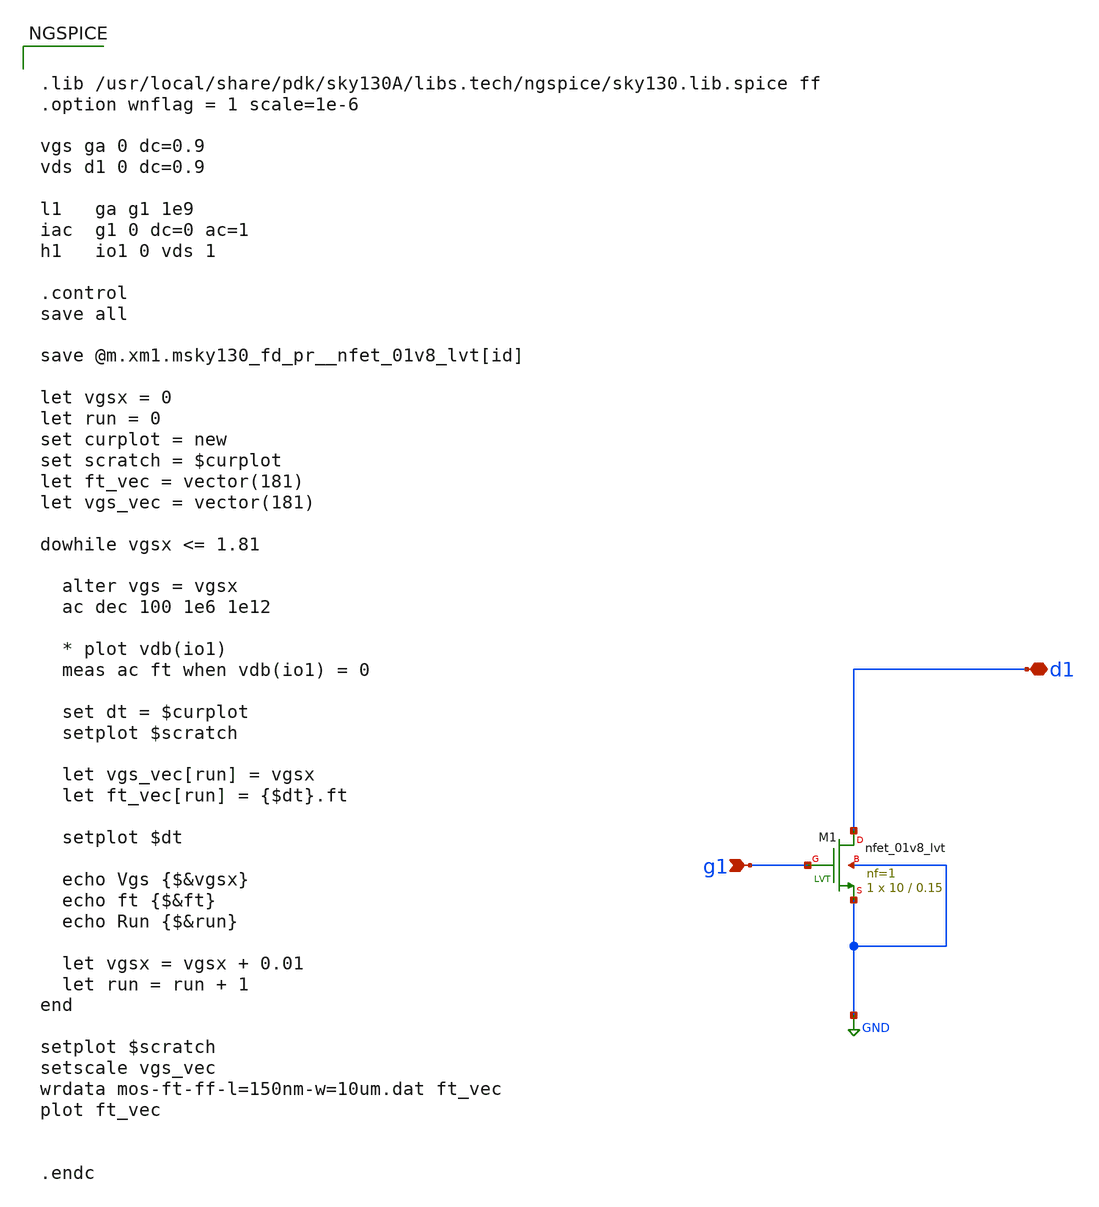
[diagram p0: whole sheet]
** sch_path: cidr/ee-220-activity-5.sch
**.subckt ee-220-activity-5 g1 d1
*.ipin g1
*.iopin d1
XM1 d1 g1 GND GND sky130_fd_pr__nfet_01v8_lvt L=0.15 W=10 nf=1 ad='int((nf+1)/2) * W/nf * 0.29' as='int((nf+2)/2) * W/nf * 0.29'
+ pd='2*int((nf+1)/2) * (W/nf + 0.29)' ps='2*int((nf+2)/2) * (W/nf + 0.29)' nrd='0.29 / W' nrs='0.29 / W'
+ sa=0 sb=0 sd=0 mult=1 m=1
**** begin user architecture code


.lib /usr/local/share/pdk/sky130A/libs.tech/ngspice/sky130.lib.spice ff
.option wnflag = 1 scale=1e-6

vgs ga 0 dc=0.9
vds d1 0 dc=0.9

l1   ga g1 1e9
iac  g1 0 dc=0 ac=1
h1   io1 0 vds 1

.control
save all

save @m.xm1.msky130_fd_pr__nfet_01v8_lvt[id]

let vgsx = 0
let run = 0
set curplot = new
set scratch = $curplot
let ft_vec = vector(181)
let vgs_vec = vector(181)

dowhile vgsx <= 1.81

  alter vgs = vgsx
  ac dec 100 1e6 1e12

  * plot vdb(io1)
  meas ac ft when vdb(io1) = 0

  set dt = $curplot
  setplot $scratch

  let vgs_vec[run] = vgsx
  let ft_vec[run] = {$dt}.ft

  setplot $dt

  echo Vgs {$&vgsx}
  echo ft {$&ft}
  echo Run {$&run}

  let vgsx = vgsx + 0.01
  let run = run + 1
end

setplot $scratch
setscale vgs_vec
wrdata mos-ft-ff-l=150nm-w=10um.dat ft_vec
plot ft_vec


.endc


**** end user architecture code
**.ends
.GLOBAL GND
.end
